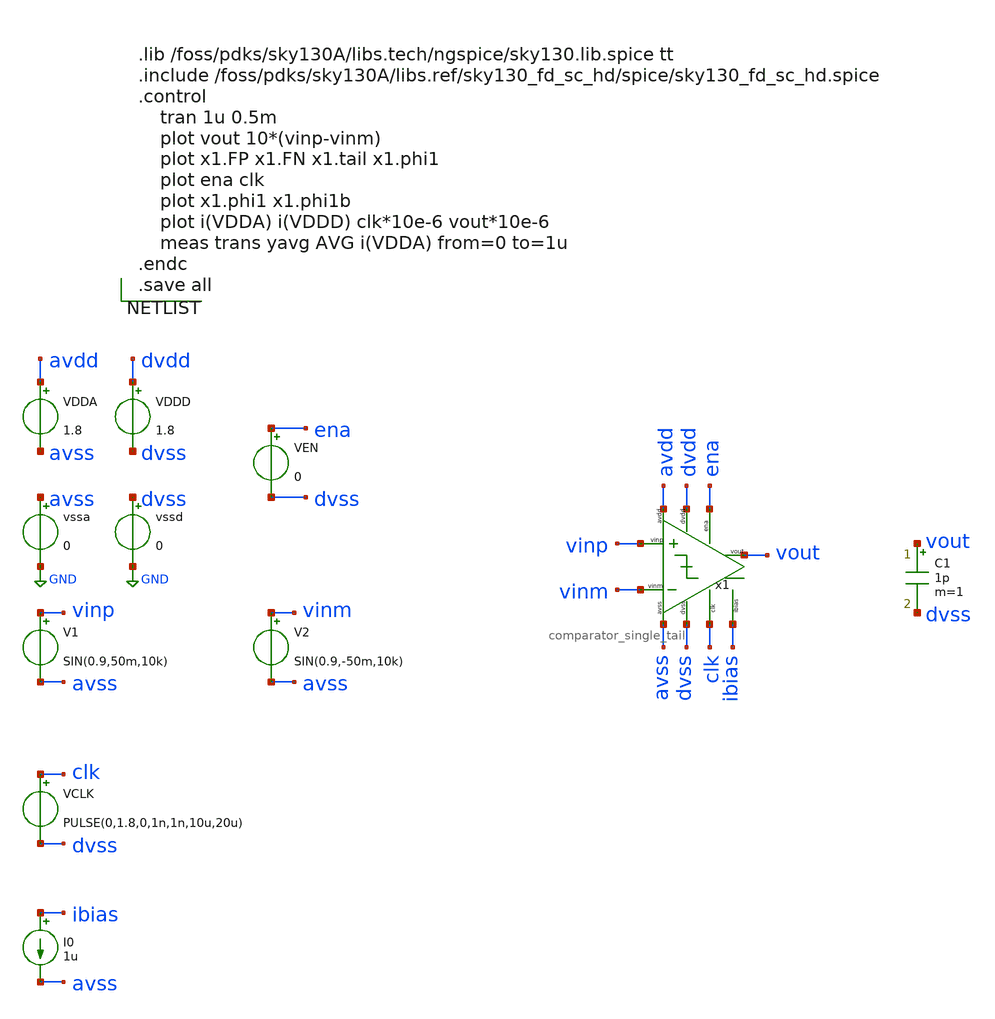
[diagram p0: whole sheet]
** sch_path: xschem/comparator_tb.sch
**.subckt comparator_tb
V1 vinp avss SIN(0.9,50m,10k)
VDDD dvdd dvss 1.8
V2 vinm avss SIN(0.9,-50m,10k)
VCLK clk dvss PULSE(0,1.8,0,1n,1n,10u,20u)
VDDA avdd avss 1.8
VEN ena dvss 0
I0 ibias avss 1u
vssa avss GND 0
vssd dvss GND 0
x1 vinp vinm vout dvdd dvss avdd avss ena clk ibias comparator_single_tail
C1 vout dvss 1p m=1
**** begin user architecture code


.lib /foss/pdks/sky130A/libs.tech/ngspice/sky130.lib.spice tt
.include /foss/pdks/sky130A/libs.ref/sky130_fd_sc_hd/spice/sky130_fd_sc_hd.spice
.control
    tran 1u 0.5m
    plot vout 10*(vinp-vinm)
    plot x1.FP x1.FN x1.tail x1.phi1
    plot ena clk
    plot x1.phi1 x1.phi1b
    plot i(VDDA) i(VDDD) clk*10e-6 vout*10e-6
    meas trans yavg AVG i(VDDA) from=0 to=1u
.endc
.save all


**** end user architecture code
**.ends

* expanding   symbol:
*+  /foss/designs/sky130_rhythmic_ip__dynamic_comparator/xschem/comparator_single_tail.sym # of pins=10
** sym_path: xschem/comparator_single_tail.sym
** sch_path: xschem/comparator_single_tail.sch
.subckt comparator_single_tail vinp vinm vout dvdd dvss avdd avss ena clk ibias
*.ipin clk
*.iopin vinp
*.iopin vinm
*.iopin dvdd
*.iopin dvss
*.opin vout
*.iopin avdd
*.iopin avss
*.iopin ibias
*.ipin ena
XM12 FP vinp tail avss sky130_fd_pr__nfet_03v3_nvt L=0.5 W=1 nf=1 ad='int((nf+1)/2) * W/nf * 0.29' as='int((nf+2)/2) * W/nf * 0.29'
+ pd='2*int((nf+1)/2) * (W/nf + 0.29)' ps='2*int((nf+2)/2) * (W/nf + 0.29)' nrd='0.29 / W' nrs='0.29 / W'
+ sa=0 sb=0 sd=0 mult=1 m=1
XM13 FN vinm tail avss sky130_fd_pr__nfet_03v3_nvt L=0.5 W=1 nf=1 ad='int((nf+1)/2) * W/nf * 0.29' as='int((nf+2)/2) * W/nf * 0.29'
+ pd='2*int((nf+1)/2) * (W/nf + 0.29)' ps='2*int((nf+2)/2) * (W/nf + 0.29)' nrd='0.29 / W' nrs='0.29 / W'
+ sa=0 sb=0 sd=0 mult=1 m=1
XM14 pfetw low dvdd dvdd sky130_fd_pr__pfet_01v8 L=0.15 W=0.42 nf=1 ad='int((nf+1)/2) * W/nf * 0.29'
+ as='int((nf+2)/2) * W/nf * 0.29' pd='2*int((nf+1)/2) * (W/nf + 0.29)' ps='2*int((nf+2)/2) * (W/nf + 0.29)'
+ nrd='0.29 / W' nrs='0.29 / W' sa=0 sb=0 sd=0 mult=1 m=1
XM3 high FP pfetw dvdd sky130_fd_pr__pfet_01v8 L=0.15 W=1 nf=1 ad='int((nf+1)/2) * W/nf * 0.29' as='int((nf+2)/2) * W/nf * 0.29'
+ pd='2*int((nf+1)/2) * (W/nf + 0.29)' ps='2*int((nf+2)/2) * (W/nf + 0.29)' nrd='0.29 / W' nrs='0.29 / W'
+ sa=0 sb=0 sd=0 mult=1 m=1
XM8 pfete FN low dvdd sky130_fd_pr__pfet_01v8 L=0.15 W=1 nf=1 ad='int((nf+1)/2) * W/nf * 0.29' as='int((nf+2)/2) * W/nf * 0.29'
+ pd='2*int((nf+1)/2) * (W/nf + 0.29)' ps='2*int((nf+2)/2) * (W/nf + 0.29)' nrd='0.29 / W' nrs='0.29 / W'
+ sa=0 sb=0 sd=0 mult=1 m=1
XM2 dvdd high pfete dvdd sky130_fd_pr__pfet_01v8 L=0.15 W=0.42 nf=1 ad='int((nf+1)/2) * W/nf * 0.29'
+ as='int((nf+2)/2) * W/nf * 0.29' pd='2*int((nf+1)/2) * (W/nf + 0.29)' ps='2*int((nf+2)/2) * (W/nf + 0.29)'
+ nrd='0.29 / W' nrs='0.29 / W' sa=0 sb=0 sd=0 mult=1 m=1
XM7 low high dvss dvss sky130_fd_pr__nfet_01v8_lvt L=2 W=0.42 nf=1 ad='int((nf+1)/2) * W/nf * 0.29' as='int((nf+2)/2) * W/nf * 0.29'
+ pd='2*int((nf+1)/2) * (W/nf + 0.29)' ps='2*int((nf+2)/2) * (W/nf + 0.29)' nrd='0.29 / W' nrs='0.29 / W'
+ sa=0 sb=0 sd=0 mult=1 m=1
XM9 high low dvss dvss sky130_fd_pr__nfet_01v8_lvt L=2 W=0.42 nf=1 ad='int((nf+1)/2) * W/nf * 0.29' as='int((nf+2)/2) * W/nf * 0.29'
+ pd='2*int((nf+1)/2) * (W/nf + 0.29)' ps='2*int((nf+2)/2) * (W/nf + 0.29)' nrd='0.29 / W' nrs='0.29 / W'
+ sa=0 sb=0 sd=0 mult=1 m=1
XM10 tail phi1 ibias avss sky130_fd_pr__nfet_01v8_lvt L=2 W=0.42 nf=1 ad='int((nf+1)/2) * W/nf * 0.29'
+ as='int((nf+2)/2) * W/nf * 0.29' pd='2*int((nf+1)/2) * (W/nf + 0.29)' ps='2*int((nf+2)/2) * (W/nf + 0.29)'
+ nrd='0.29 / W' nrs='0.29 / W' sa=0 sb=0 sd=0 mult=1 m=1
XM1 avdd phi1 FP avdd sky130_fd_pr__pfet_01v8 L=0.15 W=0.42 nf=1 ad='int((nf+1)/2) * W/nf * 0.29' as='int((nf+2)/2) * W/nf * 0.29'
+ pd='2*int((nf+1)/2) * (W/nf + 0.29)' ps='2*int((nf+2)/2) * (W/nf + 0.29)' nrd='0.29 / W' nrs='0.29 / W'
+ sa=0 sb=0 sd=0 mult=1 m=1
XM6 FN phi1 avdd avdd sky130_fd_pr__pfet_01v8 L=0.15 W=0.42 nf=1 ad='int((nf+1)/2) * W/nf * 0.29' as='int((nf+2)/2) * W/nf * 0.29'
+ pd='2*int((nf+1)/2) * (W/nf + 0.29)' ps='2*int((nf+2)/2) * (W/nf + 0.29)' nrd='0.29 / W' nrs='0.29 / W'
+ sa=0 sb=0 sd=0 mult=1 m=1
XM4 high phi1b dvss dvss sky130_fd_pr__nfet_01v8_lvt L=2 W=0.42 nf=1 ad='int((nf+1)/2) * W/nf * 0.29'
+ as='int((nf+2)/2) * W/nf * 0.29' pd='2*int((nf+1)/2) * (W/nf + 0.29)' ps='2*int((nf+2)/2) * (W/nf + 0.29)'
+ nrd='0.29 / W' nrs='0.29 / W' sa=0 sb=0 sd=0 mult=1 m=1
XM5 low phi1b dvss dvss sky130_fd_pr__nfet_01v8_lvt L=2 W=0.42 nf=1 ad='int((nf+1)/2) * W/nf * 0.29'
+ as='int((nf+2)/2) * W/nf * 0.29' pd='2*int((nf+1)/2) * (W/nf + 0.29)' ps='2*int((nf+2)/2) * (W/nf + 0.29)'
+ nrd='0.29 / W' nrs='0.29 / W' sa=0 sb=0 sd=0 mult=1 m=1
x2 high dvss dvss dvdd dvdd vout sky130_fd_sc_hd__buf_1
x3 low dvss dvss dvdd dvdd net1 sky130_fd_sc_hd__buf_1
x4 clk net3 dvss dvss dvdd dvdd net2 sky130_fd_sc_hd__dlclkp_1
x1 net2 dvss dvss dvdd dvdd phi1 sky130_fd_sc_hd__clkbuf_1
x5 net2 dvss dvss dvdd dvdd phi1b sky130_fd_sc_hd__clkinv_1
x6 ena dvss dvss dvdd dvdd net3 sky130_fd_sc_hd__inv_1
.ends

.GLOBAL GND
.end
